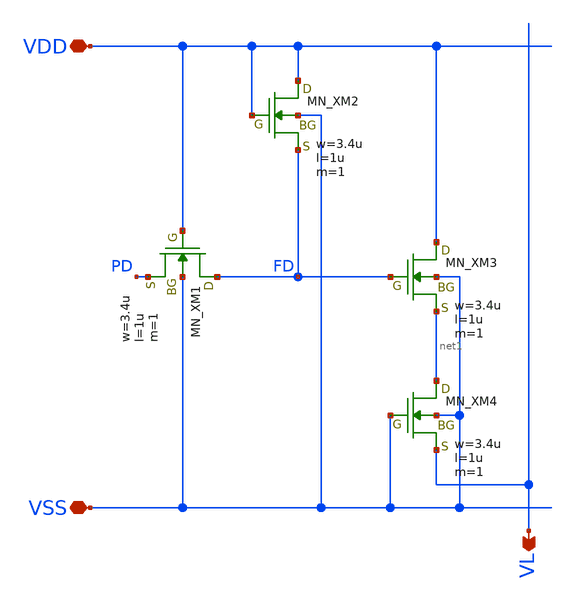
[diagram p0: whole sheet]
** sch_path: member_project/imager/YuMaehashi/design/pix_unit_dum.sch
**.subckt pix_unit_dum VDD VL VSS
*.iopin VDD
*.opin VL
*.iopin VSS
XXM1 FD VDD PD VSS NMOS w=3.4u l=1u nrd=0 nrs=0 m=1
XXM2 VDD VDD FD VSS NMOS w=3.4u l=1u nrd=0 nrs=0 m=1
XXM3 VDD FD net1 VSS NMOS w=3.4u l=1u nrd=0 nrs=0 m=1
XXM4 net1 VSS VL VSS NMOS w=3.4u l=1u nrd=0 nrs=0 m=1
**.ends
.end
